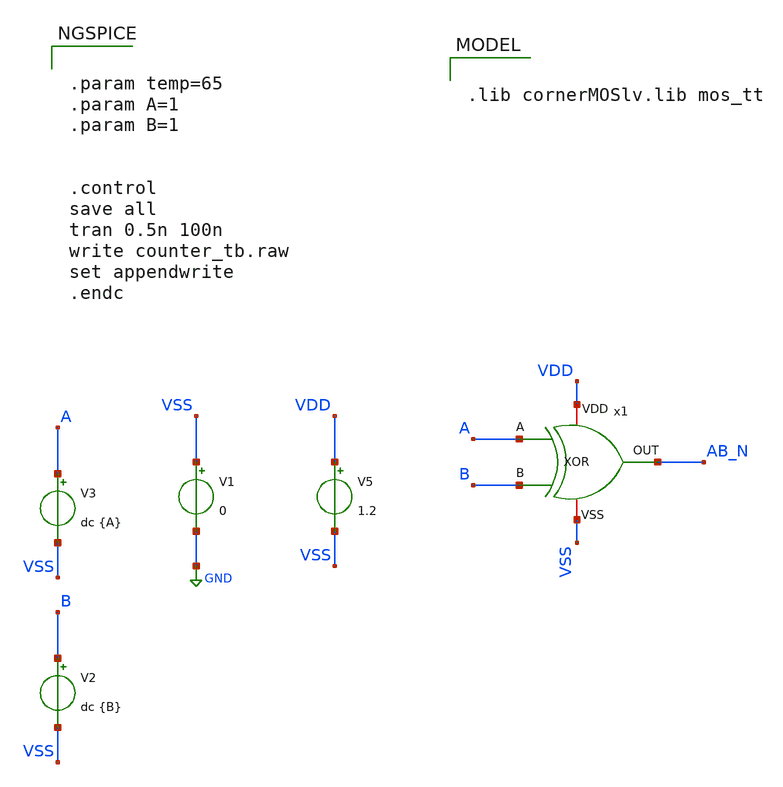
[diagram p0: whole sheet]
** sch_path: ADC8711-main/testbenches/tran/xschem/tb_XOR.sch
**.subckt tb_XOR
V1 VSS GND 0
V3 A VSS dc {A}
V5 VDD VSS 1.2
V2 B VSS dc {B}
x1 AB_N A VDD B VSS XOR
**** begin user architecture code


.param temp=65
.param A=1
.param B=1


.control
save all
tran 0.5n 100n
write counter_tb.raw
set appendwrite
.endc



.lib cornerMOSlv.lib mos_tt

**** end user architecture code
**.ends
.GLOBAL GND
.end
